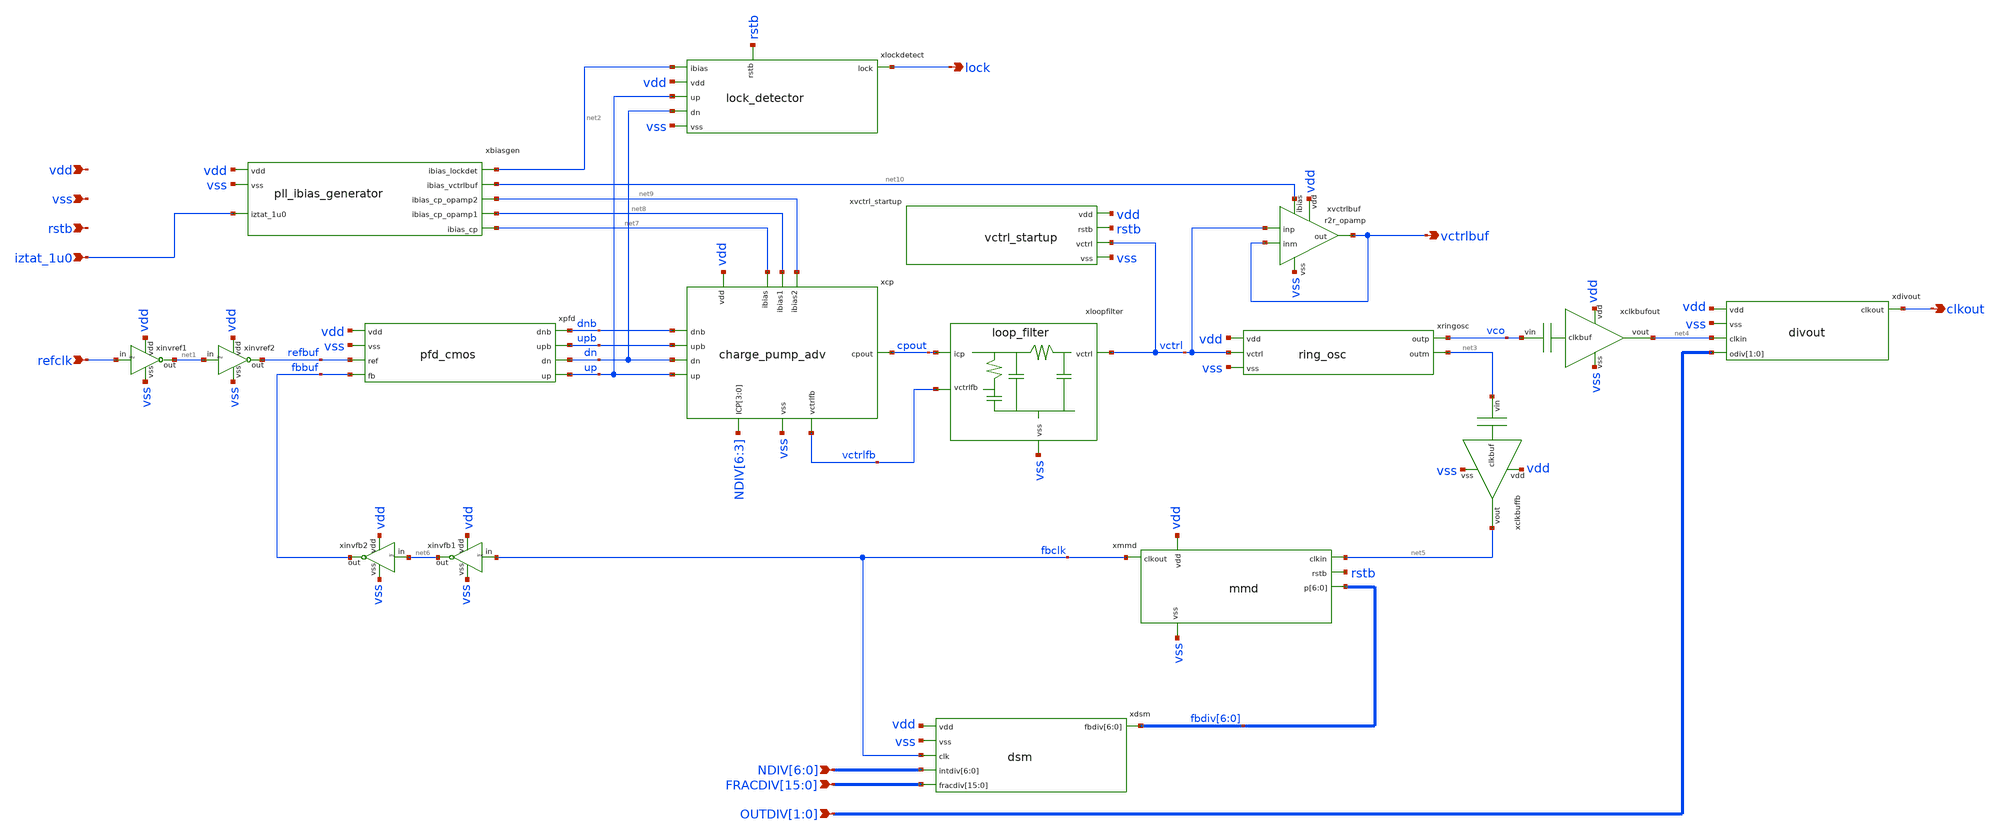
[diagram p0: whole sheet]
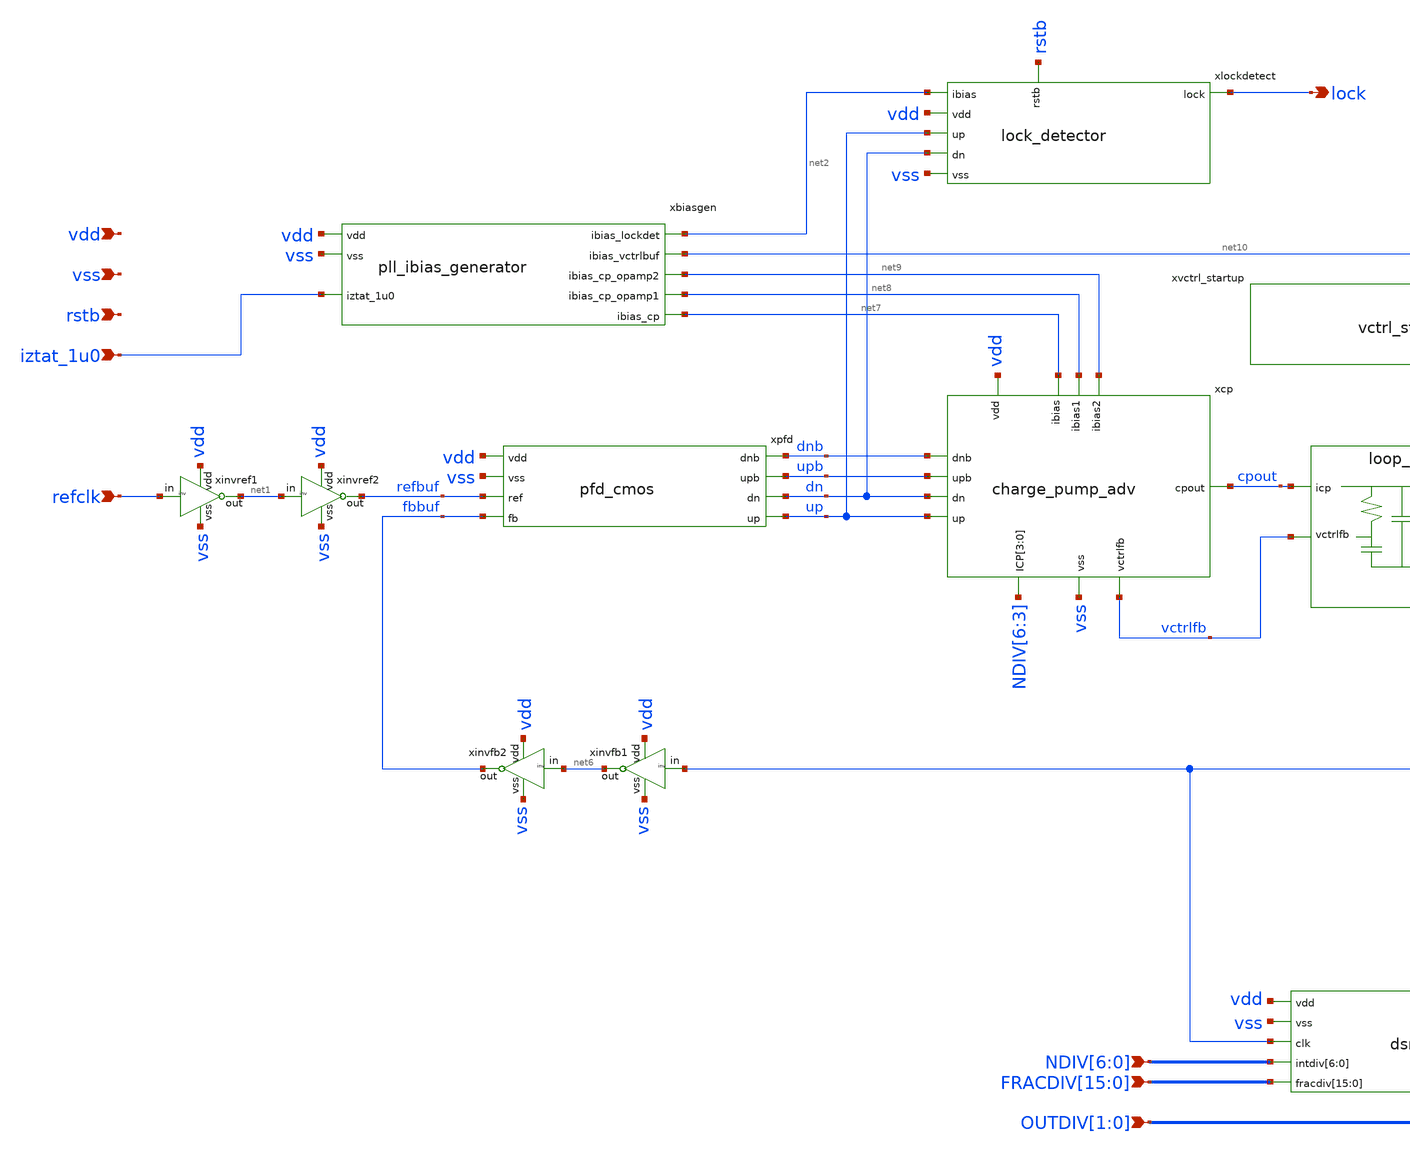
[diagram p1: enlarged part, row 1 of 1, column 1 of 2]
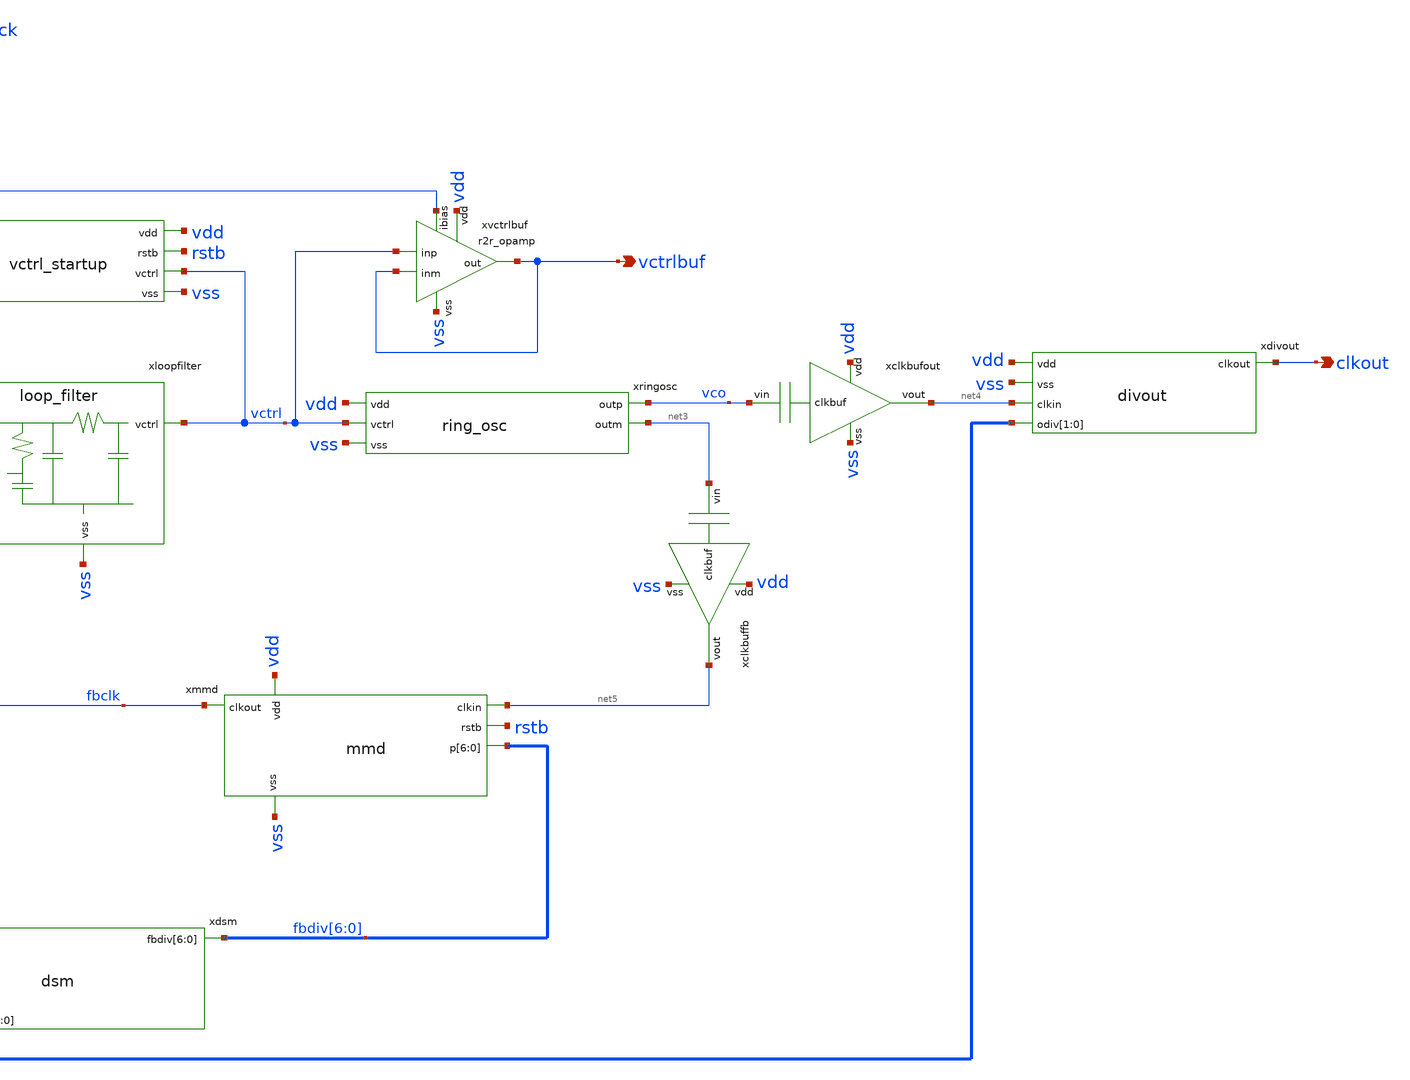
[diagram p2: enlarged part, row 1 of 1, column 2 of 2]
** sch_path: xschem/gf180mcu_tjd_ip__rofncppll.sch
**.subckt gf180mcu_tjd_ip__rofncppll refclk lock vctrlbuf vdd vss clkout
*+ NDIV[6],NDIV[5],NDIV[4],NDIV[3],NDIV[2],NDIV[1],NDIV[0]
*+ FRACDIV[15],FRACDIV[14],FRACDIV[13],FRACDIV[12],FRACDIV[11],FRACDIV[10],FRACDIV[9],FRACDIV[8],FRACDIV[7],FRACDIV[6],FRACDIV[5],FRACDIV[4],FRACDIV[3],FRACDIV[2],FRACDIV[1],FRACDIV[0] OUTDIV[1],OUTDIV[0] iztat_1u0 rstb
*.ipin refclk
*.opin lock
*.opin vctrlbuf
*.ipin vdd
*.ipin vss
*.opin clkout
*.ipin NDIV[6],NDIV[5],NDIV[4],NDIV[3],NDIV[2],NDIV[1],NDIV[0]
*.ipin
*+ FRACDIV[15],FRACDIV[14],FRACDIV[13],FRACDIV[12],FRACDIV[11],FRACDIV[10],FRACDIV[9],FRACDIV[8],FRACDIV[7],FRACDIV[6],FRACDIV[5],FRACDIV[4],FRACDIV[3],FRACDIV[2],FRACDIV[1],FRACDIV[0]
*.ipin OUTDIV[1],OUTDIV[0]
*.ipin iztat_1u0
*.ipin rstb
xinvref1 vdd refclk net1 vss inv
xinvref2 vdd net1 refbuf vss inv
xpfd vdd vss dnb upb refbuf fbbuf dn up pfd_cmos
xcp vdd up upb net8 net9 cpout net7 dnb dn vss vctrlfb NDIV[6] NDIV[5] NDIV[4] NDIV[3]
+ charge_pump_adv
xlockdetect net2 vdd up dn lock vss rstb lock_detector
xringosc vco net3 vdd vctrl vss ring_osc
xdivout vdd vss clkout net4 OUTDIV[1] OUTDIV[0] divout
xclkbuffb vdd net3 net5 vss clkbuf
xclkbufout vdd vco net4 vss clkbuf
xmmd fbclk net5 vdd vss rstb fbdiv[6] fbdiv[5] fbdiv[4] fbdiv[3] fbdiv[2] fbdiv[1] fbdiv[0] mmd
xloopfilter cpout vctrl vctrlfb vss loop_filter
xvctrlbuf vdd vctrlbuf net10 vctrl vctrlbuf vss r2r_opamp
xinvfb1 vdd fbclk net6 vss inv
xinvfb2 vdd net6 fbbuf vss inv
xdsm vdd vss fbclk NDIV[6] NDIV[5] NDIV[4] NDIV[3] NDIV[2] NDIV[1] NDIV[0] FRACDIV[15] FRACDIV[14]
+ FRACDIV[13] FRACDIV[12] FRACDIV[11] FRACDIV[10] FRACDIV[9] FRACDIV[8] FRACDIV[7] FRACDIV[6] FRACDIV[5]
+ FRACDIV[4] FRACDIV[3] FRACDIV[2] FRACDIV[1] FRACDIV[0] fbdiv[6] fbdiv[5] fbdiv[4] fbdiv[3] fbdiv[2] fbdiv[1]
+ fbdiv[0] dsm
xbiasgen vdd iztat_1u0 net2 net10 net9 net8 net7 vss pll_ibias_generator
xvctrl_startup vdd rstb vctrl vss vctrl_startup
**.ends
.end
